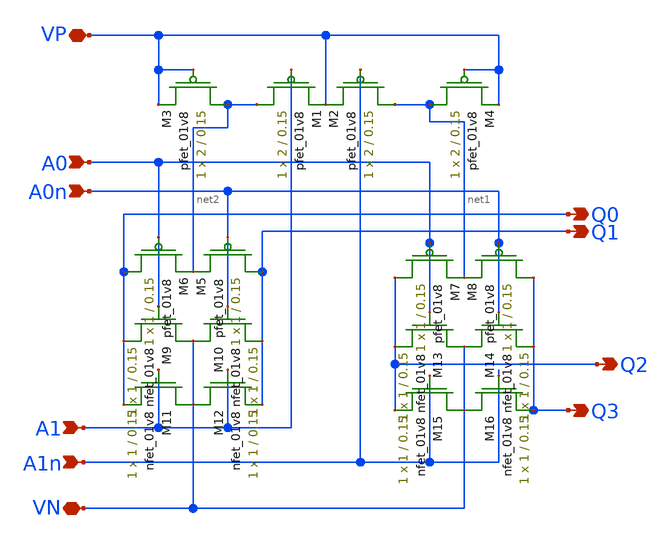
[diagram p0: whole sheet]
** sch_path: DRAM_Components/Schematic/PreDecode.sch
**.subckt PreDecode A0 A0n A1 A1n Q0 Q1 Q2 Q3 VP VN
*.ipin A0
*.ipin A0n
*.ipin A1
*.ipin A1n
*.opin Q0
*.opin Q1
*.opin Q2
*.opin Q3
*.iopin VP
*.iopin VN
XM2 net1 A1n VP VP sky130_fd_pr__pfet_01v8 L=0.15 W=2 nf=1 ad='int((nf+1)/2) * W/nf * 0.29' as='int((nf+2)/2) * W/nf * 0.29'
+ pd='2*int((nf+1)/2) * (W/nf + 0.29)' ps='2*int((nf+2)/2) * (W/nf + 0.29)' nrd='0.29 / W' nrs='0.29 / W'
+ sa=0 sb=0 sd=0 mult=1 m=1
XM1 net2 A1 VP VP sky130_fd_pr__pfet_01v8 L=0.15 W=2 nf=1 ad='int((nf+1)/2) * W/nf * 0.29' as='int((nf+2)/2) * W/nf * 0.29'
+ pd='2*int((nf+1)/2) * (W/nf + 0.29)' ps='2*int((nf+2)/2) * (W/nf + 0.29)' nrd='0.29 / W' nrs='0.29 / W'
+ sa=0 sb=0 sd=0 mult=1 m=1
XM3 net2 VP VP VP sky130_fd_pr__pfet_01v8 L=0.15 W=2 nf=1 ad='int((nf+1)/2) * W/nf * 0.29' as='int((nf+2)/2) * W/nf * 0.29'
+ pd='2*int((nf+1)/2) * (W/nf + 0.29)' ps='2*int((nf+2)/2) * (W/nf + 0.29)' nrd='0.29 / W' nrs='0.29 / W'
+ sa=0 sb=0 sd=0 mult=1 m=1
XM4 net1 VP VP VP sky130_fd_pr__pfet_01v8 L=0.15 W=2 nf=1 ad='int((nf+1)/2) * W/nf * 0.29' as='int((nf+2)/2) * W/nf * 0.29'
+ pd='2*int((nf+1)/2) * (W/nf + 0.29)' ps='2*int((nf+2)/2) * (W/nf + 0.29)' nrd='0.29 / W' nrs='0.29 / W'
+ sa=0 sb=0 sd=0 mult=1 m=1
XM5 Q1 A0n net2 VP sky130_fd_pr__pfet_01v8 L=0.15 W=1 nf=1 ad='int((nf+1)/2) * W/nf * 0.29' as='int((nf+2)/2) * W/nf * 0.29'
+ pd='2*int((nf+1)/2) * (W/nf + 0.29)' ps='2*int((nf+2)/2) * (W/nf + 0.29)' nrd='0.29 / W' nrs='0.29 / W'
+ sa=0 sb=0 sd=0 mult=1 m=1
XM6 Q0 A0 net2 VP sky130_fd_pr__pfet_01v8 L=0.15 W=1 nf=1 ad='int((nf+1)/2) * W/nf * 0.29' as='int((nf+2)/2) * W/nf * 0.29'
+ pd='2*int((nf+1)/2) * (W/nf + 0.29)' ps='2*int((nf+2)/2) * (W/nf + 0.29)' nrd='0.29 / W' nrs='0.29 / W'
+ sa=0 sb=0 sd=0 mult=1 m=1
XM7 Q2 A0 net1 VP sky130_fd_pr__pfet_01v8 L=0.15 W=1 nf=1 ad='int((nf+1)/2) * W/nf * 0.29' as='int((nf+2)/2) * W/nf * 0.29'
+ pd='2*int((nf+1)/2) * (W/nf + 0.29)' ps='2*int((nf+2)/2) * (W/nf + 0.29)' nrd='0.29 / W' nrs='0.29 / W'
+ sa=0 sb=0 sd=0 mult=1 m=1
XM8 Q3 A0n net1 VP sky130_fd_pr__pfet_01v8 L=0.15 W=1 nf=1 ad='int((nf+1)/2) * W/nf * 0.29' as='int((nf+2)/2) * W/nf * 0.29'
+ pd='2*int((nf+1)/2) * (W/nf + 0.29)' ps='2*int((nf+2)/2) * (W/nf + 0.29)' nrd='0.29 / W' nrs='0.29 / W'
+ sa=0 sb=0 sd=0 mult=1 m=1
XM9 VN A0 Q0 VN sky130_fd_pr__nfet_01v8 L=0.15 W=1 nf=1 ad='int((nf+1)/2) * W/nf * 0.29' as='int((nf+2)/2) * W/nf * 0.29'
+ pd='2*int((nf+1)/2) * (W/nf + 0.29)' ps='2*int((nf+2)/2) * (W/nf + 0.29)' nrd='0.29 / W' nrs='0.29 / W'
+ sa=0 sb=0 sd=0 mult=1 m=1
XM10 VN A0n Q1 VN sky130_fd_pr__nfet_01v8 L=0.15 W=1 nf=1 ad='int((nf+1)/2) * W/nf * 0.29' as='int((nf+2)/2) * W/nf * 0.29'
+ pd='2*int((nf+1)/2) * (W/nf + 0.29)' ps='2*int((nf+2)/2) * (W/nf + 0.29)' nrd='0.29 / W' nrs='0.29 / W'
+ sa=0 sb=0 sd=0 mult=1 m=1
XM11 VN A1 Q0 VN sky130_fd_pr__nfet_01v8 L=0.15 W=1 nf=1 ad='int((nf+1)/2) * W/nf * 0.29' as='int((nf+2)/2) * W/nf * 0.29'
+ pd='2*int((nf+1)/2) * (W/nf + 0.29)' ps='2*int((nf+2)/2) * (W/nf + 0.29)' nrd='0.29 / W' nrs='0.29 / W'
+ sa=0 sb=0 sd=0 mult=1 m=1
XM12 VN A1 Q1 VN sky130_fd_pr__nfet_01v8 L=0.15 W=1 nf=1 ad='int((nf+1)/2) * W/nf * 0.29' as='int((nf+2)/2) * W/nf * 0.29'
+ pd='2*int((nf+1)/2) * (W/nf + 0.29)' ps='2*int((nf+2)/2) * (W/nf + 0.29)' nrd='0.29 / W' nrs='0.29 / W'
+ sa=0 sb=0 sd=0 mult=1 m=1
XM13 VN A0 Q2 VN sky130_fd_pr__nfet_01v8 L=0.15 W=1 nf=1 ad='int((nf+1)/2) * W/nf * 0.29' as='int((nf+2)/2) * W/nf * 0.29'
+ pd='2*int((nf+1)/2) * (W/nf + 0.29)' ps='2*int((nf+2)/2) * (W/nf + 0.29)' nrd='0.29 / W' nrs='0.29 / W'
+ sa=0 sb=0 sd=0 mult=1 m=1
XM14 VN A0n Q3 VN sky130_fd_pr__nfet_01v8 L=0.15 W=1 nf=1 ad='int((nf+1)/2) * W/nf * 0.29' as='int((nf+2)/2) * W/nf * 0.29'
+ pd='2*int((nf+1)/2) * (W/nf + 0.29)' ps='2*int((nf+2)/2) * (W/nf + 0.29)' nrd='0.29 / W' nrs='0.29 / W'
+ sa=0 sb=0 sd=0 mult=1 m=1
XM15 VN A1n Q2 VN sky130_fd_pr__nfet_01v8 L=0.15 W=1 nf=1 ad='int((nf+1)/2) * W/nf * 0.29' as='int((nf+2)/2) * W/nf * 0.29'
+ pd='2*int((nf+1)/2) * (W/nf + 0.29)' ps='2*int((nf+2)/2) * (W/nf + 0.29)' nrd='0.29 / W' nrs='0.29 / W'
+ sa=0 sb=0 sd=0 mult=1 m=1
XM16 VN A1n Q3 VN sky130_fd_pr__nfet_01v8 L=0.15 W=1 nf=1 ad='int((nf+1)/2) * W/nf * 0.29' as='int((nf+2)/2) * W/nf * 0.29'
+ pd='2*int((nf+1)/2) * (W/nf + 0.29)' ps='2*int((nf+2)/2) * (W/nf + 0.29)' nrd='0.29 / W' nrs='0.29 / W'
+ sa=0 sb=0 sd=0 mult=1 m=1
**.ends
.end
